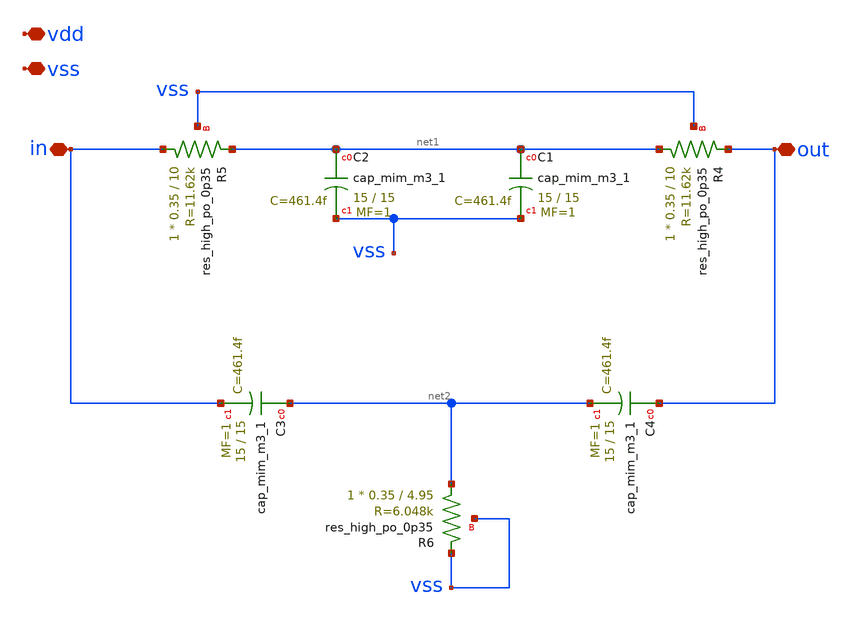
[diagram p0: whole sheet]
** sch_path: xschem/twin_tee.sch
**.subckt twin_tee vdd vss in out
*.iopin vdd
*.iopin vss
*.iopin in
*.iopin out
XR4 net1 out vss sky130_fd_pr__res_high_po_0p35 L=10 mult=1 m=1
XC1 net1 vss sky130_fd_pr__cap_mim_m3_1 W=15 L=15 MF=1 m=1
XC2 net1 vss sky130_fd_pr__cap_mim_m3_1 W=15 L=15 MF=1 m=1
XR5 in net1 vss sky130_fd_pr__res_high_po_0p35 L=10 mult=1 m=1
XC3 net2 in sky130_fd_pr__cap_mim_m3_1 W=15 L=15 MF=1 m=1
XC4 out net2 sky130_fd_pr__cap_mim_m3_1 W=15 L=15 MF=1 m=1
XR6 net2 vss vss sky130_fd_pr__res_high_po_0p35 L=4.95 mult=1 m=1
**.ends
.end
